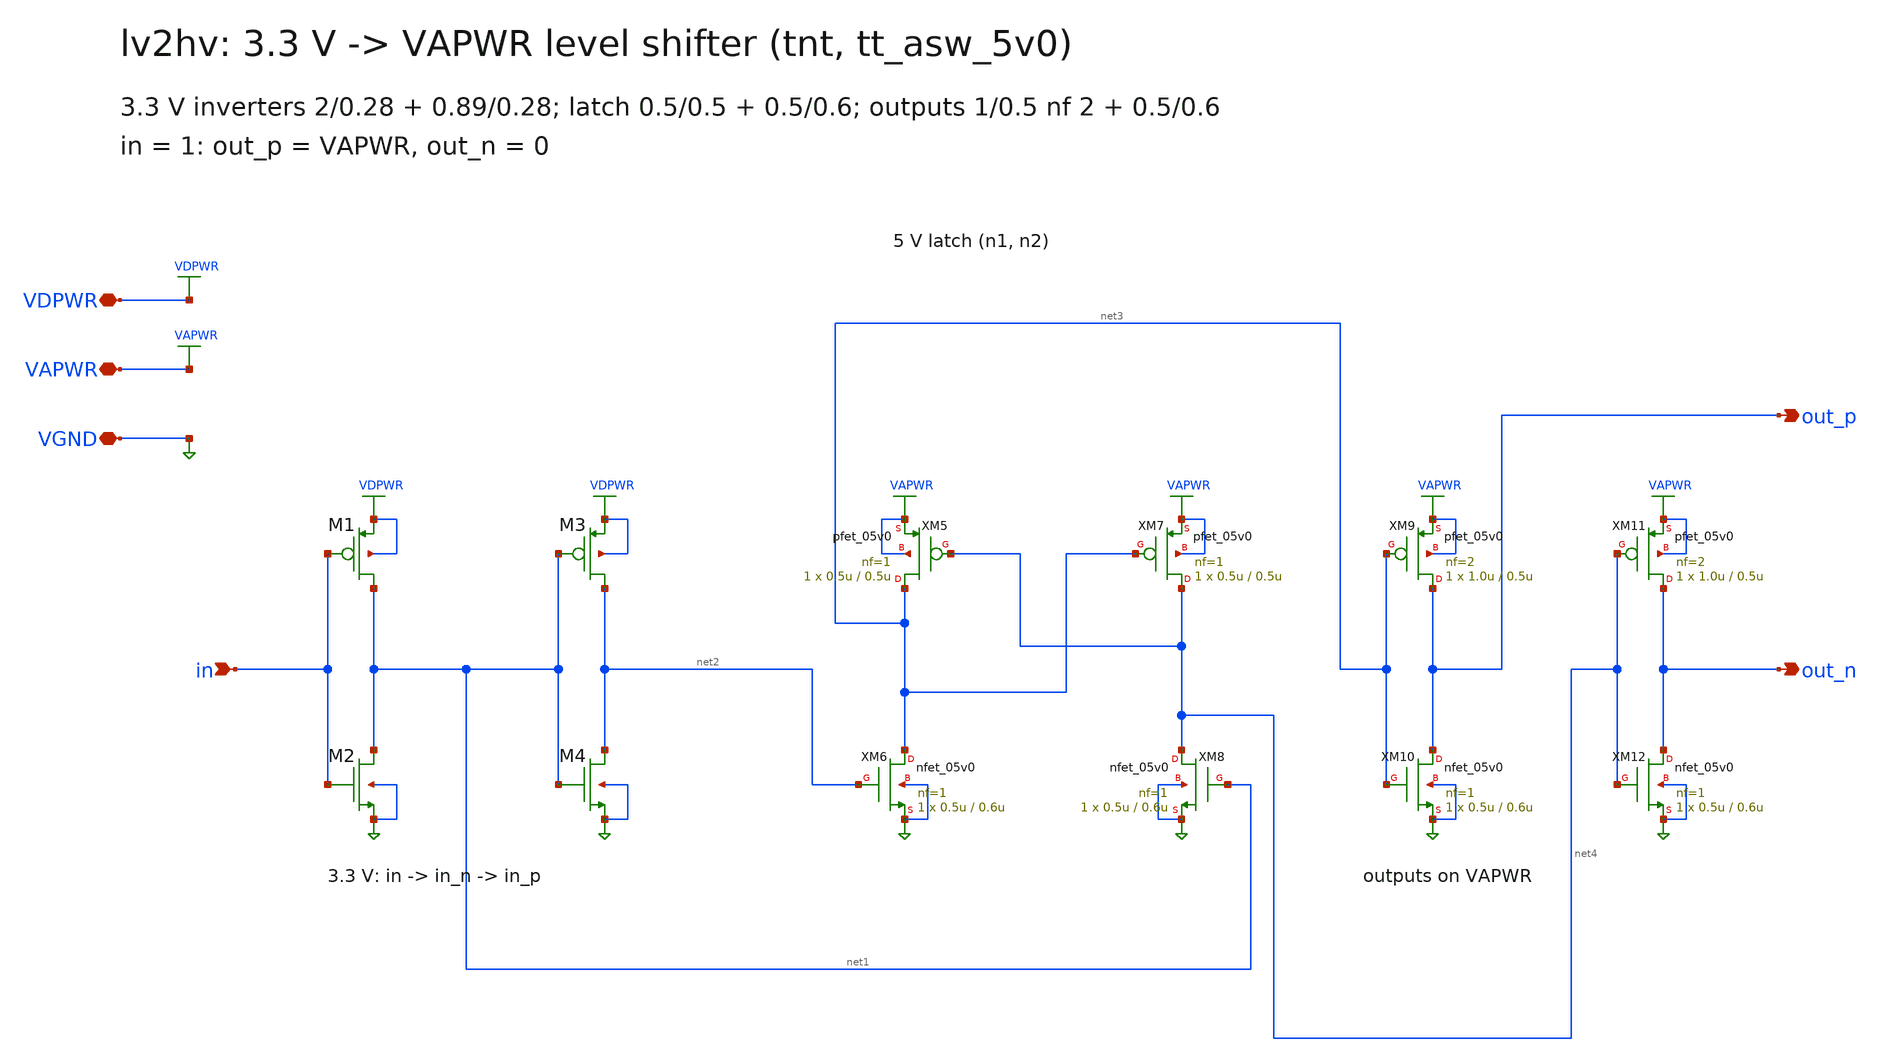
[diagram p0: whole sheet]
** sch_path: xschem/lv2hv.sch
**.subckt lv2hv VGND VDPWR VAPWR in out_p out_n
*.iopin VGND
*.iopin VDPWR
*.iopin VAPWR
*.ipin in
*.opin out_p
*.opin out_n
XM1 net1 in VDPWR VDPWR pfet_03v3 L=0.28u W=2.0u nf=1 ad=0.36p as=0.36p pd=4.36u ps=4.36u nrd=0
+ nrs=0 sa=0 sb=0 sd=0 m=1
XM2 net1 in VGND VGND nfet_03v3 L=0.28u W=0.89u nf=1 ad=0.1602p as=0.1602p pd=2.14u ps=2.14u nrd=0
+ nrs=0 sa=0 sb=0 sd=0 m=1
XM3 net2 net1 VDPWR VDPWR pfet_03v3 L=0.28u W=2.0u nf=1 ad=0.36p as=0.36p pd=4.36u ps=4.36u nrd=0
+ nrs=0 sa=0 sb=0 sd=0 m=1
XM4 net2 net1 VGND VGND nfet_03v3 L=0.28u W=0.89u nf=1 ad=0.1602p as=0.1602p pd=2.14u ps=2.14u nrd=0
+ nrs=0 sa=0 sb=0 sd=0 m=1
XM5 net3 net4 VAPWR VAPWR pfet_05v0 L=0.5u W=0.5u nf=1 ad=0.09p as=0.09p pd=1.36u ps=1.36u nrd=0
+ nrs=0 sa=0 sb=0 sd=0 m=1
XM6 net3 net2 VGND VGND nfet_05v0 L=0.6u W=0.5u nf=1 ad=0.09p as=0.09p pd=1.36u ps=1.36u nrd=0 nrs=0
+ sa=0 sb=0 sd=0 m=1
XM7 net4 net3 VAPWR VAPWR pfet_05v0 L=0.5u W=0.5u nf=1 ad=0.09p as=0.09p pd=1.36u ps=1.36u nrd=0
+ nrs=0 sa=0 sb=0 sd=0 m=1
XM8 net4 net1 VGND VGND nfet_05v0 L=0.6u W=0.5u nf=1 ad=0.09p as=0.09p pd=1.36u ps=1.36u nrd=0 nrs=0
+ sa=0 sb=0 sd=0 m=1
XM9 out_p net3 VAPWR VAPWR pfet_05v0 L=0.5u W=1.0u nf=2 ad=0.09p as=0.18p pd=1.36u ps=2.72u nrd=0
+ nrs=0 sa=0 sb=0 sd=0 m=1
XM10 out_p net3 VGND VGND nfet_05v0 L=0.6u W=0.5u nf=1 ad=0.09p as=0.09p pd=1.36u ps=1.36u nrd=0
+ nrs=0 sa=0 sb=0 sd=0 m=1
XM11 out_n net4 VAPWR VAPWR pfet_05v0 L=0.5u W=1.0u nf=2 ad=0.09p as=0.18p pd=1.36u ps=2.72u nrd=0
+ nrs=0 sa=0 sb=0 sd=0 m=1
XM12 out_n net4 VGND VGND nfet_05v0 L=0.6u W=0.5u nf=1 ad=0.09p as=0.09p pd=1.36u ps=1.36u nrd=0
+ nrs=0 sa=0 sb=0 sd=0 m=1
**.ends
.end
